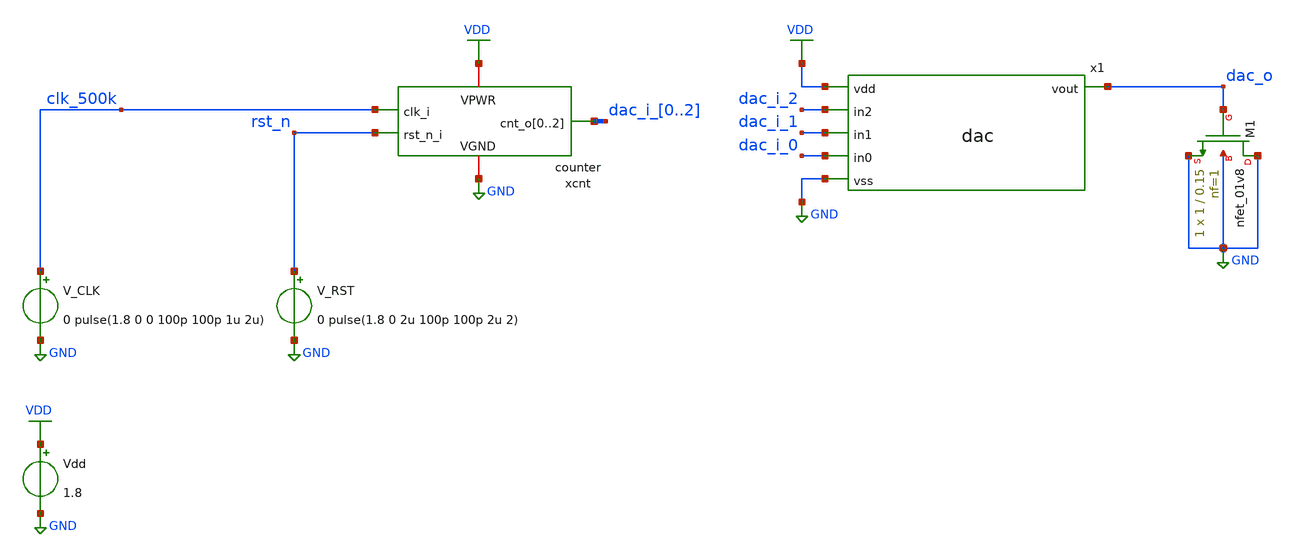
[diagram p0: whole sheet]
** sch_path: examples/3b_DAC_AMS/xschem/dac_tb.sch
**.subckt dac_tb
Vdd VDD GND 1.8
xcnt GND VDD clk_500k dac_i_0 dac_i_1 dac_i_2 rst_n counter
V_CLK clk_500k GND 0 pulse(1.8 0 0 100p 100p 1u 2u)
V_RST rst_n GND 0 pulse(1.8 0 2u 100p 100p 2u 2)
x1 VDD dac_o dac_i_2 dac_i_1 dac_i_0 GND dac
XM1 GND dac_o GND GND sky130_fd_pr__nfet_01v8 L=0.15 W=1 nf=1 ad='int((nf+1)/2) * W/nf * 0.29' as='int((nf+2)/2) * W/nf * 0.29'
+ pd='2*int((nf+1)/2) * (W/nf + 0.29)' ps='2*int((nf+2)/2) * (W/nf + 0.29)' nrd='0.29 / W' nrs='0.29 / W'
+ sa=0 sb=0 sd=0 mult=1 m=1
**** begin user architecture code
 ** manual skywater pdks install (with patches applied)
* .lib $::SKYWATER_MODELS/models/sky130.lib.spice tt

** opencircuitdesign pdks install
.lib $::SKYWATER_MODELS/sky130.lib.spice.tt.red tt

.param mc_mm_switch=0
.param mc_pr_switch=0



* ngspice commands
****************
* True mixed signal? (xspice) or analog? (spice)
****************
*.include /foss/designs/SKY130-RTL-with-Custom-Standardcell-to-GDSII/examples/3b_DAC_AMS/spice/counter.xspice
.include /foss/designs/SKY130-RTL-with-Custom-Standardcell-to-GDSII/examples/3b_DAC_AMS/spice/counter.spice

.save all
.control
set noaskquit
set num_threads=12

tran 10n 20u

write dac_tb.raw

.endc


**** end user architecture code
**.ends

* expanding   symbol:
*+  /foss/designs/SKY130-RTL-with-Custom-Standardcell-to-GDSII/examples/3b_DAC_AMS/xschem/dac.sym # of pins=6
** sym_path: examples/3b_DAC_AMS/xschem/dac.sym
** sch_path: examples/3b_DAC_AMS/xschem/dac.sch
.subckt dac vdd vout in2 in1 in0 vss
*.ipin vdd
*.ipin vss
*.opin vout
*.ipin in0
*.ipin in1
*.ipin in2
xdrv_b2 vdd in2 v2 vss dac_drv
xdrv_b1 vdd in1 v1 vss dac_drv
xdrv_b0 vdd in0 v0 vss dac_drv
XR1 net6 vout vss sky130_fd_pr__res_xhigh_po_0p35 L=1.4 mult=1 m=1
xdrv_dummy vdd vss net4 vss dac_drv
XR2 net1 v2 vss sky130_fd_pr__res_xhigh_po_0p35 L=1.4 mult=1 m=1
XR3 vout net1 vss sky130_fd_pr__res_xhigh_po_0p35 L=1.4 mult=1 m=1
.save v(vout)
.save v(v2)
.save v(v1)
.save v(v0)
XR4 net5 net6 vss sky130_fd_pr__res_xhigh_po_0p35 L=1.4 mult=1 m=1
XR5 net7 v1 vss sky130_fd_pr__res_xhigh_po_0p35 L=1.4 mult=1 m=1
XR6 net6 net7 vss sky130_fd_pr__res_xhigh_po_0p35 L=1.4 mult=1 m=1
XR8 net2 v0 vss sky130_fd_pr__res_xhigh_po_0p35 L=1.4 mult=1 m=1
XR9 net5 net2 vss sky130_fd_pr__res_xhigh_po_0p35 L=1.4 mult=1 m=1
XR10 net3 net4 vss sky130_fd_pr__res_xhigh_po_0p35 L=1.4 mult=1 m=1
XR11 net5 net3 vss sky130_fd_pr__res_xhigh_po_0p35 L=1.4 mult=1 m=1
.ends


* expanding   symbol:  dac_drv.sym # of pins=4
** sym_path: examples/3b_DAC_AMS/xschem/dac_drv.sym
** sch_path: examples/3b_DAC_AMS/xschem/dac_drv.sch
.subckt dac_drv vdd in out vss
*.ipin vdd
*.ipin vss
*.ipin in
*.opin out
XM1 net1 in vss vss sky130_fd_pr__nfet_01v8 L=0.5 W=5 nf=1 ad='int((nf+1)/2) * W/nf * 0.29' as='int((nf+2)/2) * W/nf * 0.29'
+ pd='2*int((nf+1)/2) * (W/nf + 0.29)' ps='2*int((nf+2)/2) * (W/nf + 0.29)' nrd='0.29 / W' nrs='0.29 / W'
+ sa=0 sb=0 sd=0 mult=1 m=1
XM2A net1 in vdd vdd sky130_fd_pr__pfet_01v8 L=0.5 W=5 nf=1 ad='int((nf+1)/2) * W/nf * 0.29' as='int((nf+2)/2) * W/nf * 0.29'
+ pd='2*int((nf+1)/2) * (W/nf + 0.29)' ps='2*int((nf+2)/2) * (W/nf + 0.29)' nrd='0.29 / W' nrs='0.29 / W'
+ sa=0 sb=0 sd=0 mult=1 m=1
XM4A out net1 vdd vdd sky130_fd_pr__pfet_01v8 L=0.5 W=5 nf=1 ad='int((nf+1)/2) * W/nf * 0.29' as='int((nf+2)/2) * W/nf * 0.29'
+ pd='2*int((nf+1)/2) * (W/nf + 0.29)' ps='2*int((nf+2)/2) * (W/nf + 0.29)' nrd='0.29 / W' nrs='0.29 / W'
+ sa=0 sb=0 sd=0 mult=1 m=1
XM3 out net1 vss vss sky130_fd_pr__nfet_01v8 L=0.5 W=5 nf=1 ad='int((nf+1)/2) * W/nf * 0.29' as='int((nf+2)/2) * W/nf * 0.29'
+ pd='2*int((nf+1)/2) * (W/nf + 0.29)' ps='2*int((nf+2)/2) * (W/nf + 0.29)' nrd='0.29 / W' nrs='0.29 / W'
+ sa=0 sb=0 sd=0 mult=1 m=1
XM2B net1 in vdd vdd sky130_fd_pr__pfet_01v8 L=0.5 W=5 nf=1 ad='int((nf+1)/2) * W/nf * 0.29' as='int((nf+2)/2) * W/nf * 0.29'
+ pd='2*int((nf+1)/2) * (W/nf + 0.29)' ps='2*int((nf+2)/2) * (W/nf + 0.29)' nrd='0.29 / W' nrs='0.29 / W'
+ sa=0 sb=0 sd=0 mult=1 m=1
XM4B out net1 vdd vdd sky130_fd_pr__pfet_01v8 L=0.5 W=5 nf=1 ad='int((nf+1)/2) * W/nf * 0.29' as='int((nf+2)/2) * W/nf * 0.29'
+ pd='2*int((nf+1)/2) * (W/nf + 0.29)' ps='2*int((nf+2)/2) * (W/nf + 0.29)' nrd='0.29 / W' nrs='0.29 / W'
+ sa=0 sb=0 sd=0 mult=1 m=1
.ends

.GLOBAL GND
.GLOBAL VDD
.end
